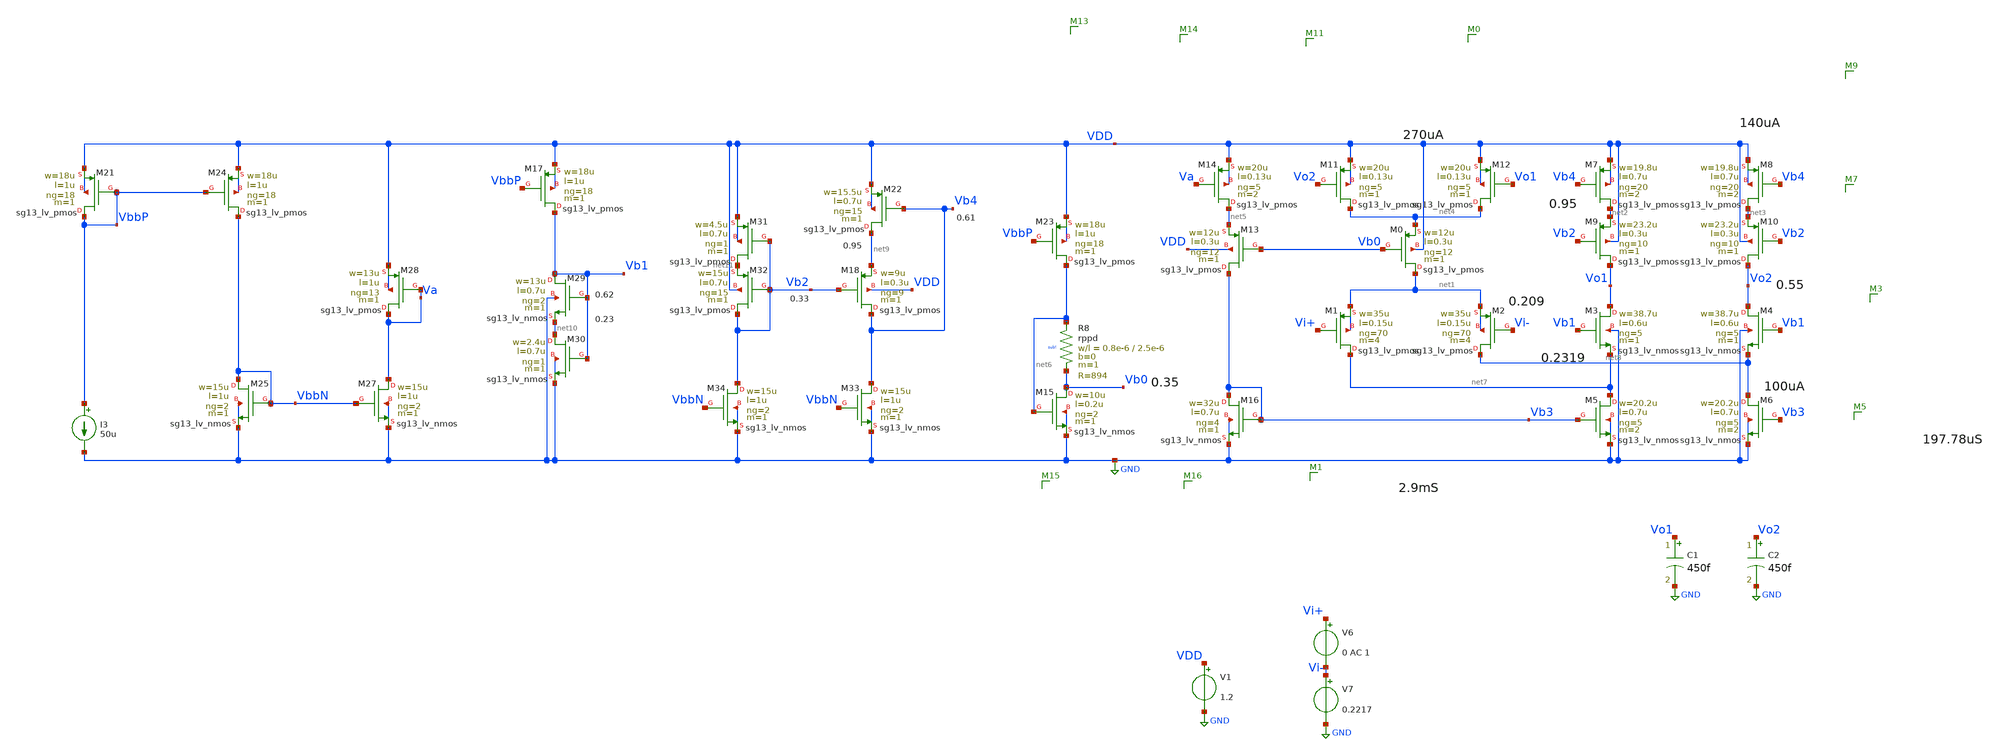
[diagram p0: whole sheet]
** sch_path: sch/testing/gmBoosting.sch
**.subckt gmBoosting
XM7 net2 Vb4 VDD VDD sg13_lv_pmos w=19.8u l=0.7u ng=20 m=2 mm_ok=1
XM1 net7 Vi+ net1 net1 sg13_lv_pmos w=35u l=0.15u ng=70 m=4 mm_ok=1
XM2 net8 Vi- net1 net1 sg13_lv_pmos w=35u l=0.15u ng=70 m=4 mm_ok=1
XM0 net1 Vb0 net4 VDD sg13_lv_pmos w=12u l=0.3u ng=12 m=1 mm_ok=1
V1 VDD GND 1.2
V7 Vi- GND 0.2217
V6 Vi+ Vi- 0 AC 1
C1 Vo1 GND 450f m=1
C2 Vo2 GND 450f m=1
XM9 Vo1 Vb2 net2 VDD sg13_lv_pmos w=23.2u l=0.3u ng=10 m=1 mm_ok=1
XM10 Vo2 Vb2 net3 VDD sg13_lv_pmos w=23.2u l=0.3u ng=10 m=1 mm_ok=1
XM8 net3 Vb4 VDD VDD sg13_lv_pmos w=19.8u l=0.7u ng=20 m=2 mm_ok=1
XM11 net4 Vo2 VDD VDD sg13_lv_pmos w=20u l=0.13u ng=5 m=1 mm_ok=1
XM12 net4 Vo1 VDD VDD sg13_lv_pmos w=20u l=0.13u ng=5 m=1 mm_ok=1
XM14 net5 Va VDD VDD sg13_lv_pmos w=20u l=0.13u ng=5 m=2 mm_ok=1
XM15 Vb0 net6 GND GND sg13_lv_nmos w=10u l=0.2u ng=2 m=1 mm_ok=1
XM16 Vb3 Vb3 GND GND sg13_lv_nmos w=32u l=0.7u ng=4 m=1 mm_ok=1
XR8 net6 Vb0 sub! rppd w=0.8e-6 l=2.5e-6 m=1 b=0 mm_ok=1
XM13 Vb3 Vb0 net5 VDD sg13_lv_pmos w=12u l=0.3u ng=12 m=1 mm_ok=1
I3 VbbP GND 50u
XM21 VbbP VbbP VDD VDD sg13_lv_pmos w=18u l=1u ng=18 m=1 mm_ok=1
XM23 net6 VbbP VDD VDD sg13_lv_pmos w=18u l=1u ng=18 m=1 mm_ok=1
XM24 VbbN VbbP VDD VDD sg13_lv_pmos w=18u l=1u ng=18 m=1 mm_ok=1
XM25 VbbN VbbN GND GND sg13_lv_nmos w=15u l=1u ng=2 m=1 mm_ok=1
XM27 Va VbbN GND GND sg13_lv_nmos w=15u l=1u ng=2 m=1 mm_ok=1
XM28 Va Va VDD VDD sg13_lv_pmos w=13u l=1u ng=13 m=1 mm_ok=1
XM29 Vb1 Vb1 net10 GND sg13_lv_nmos w=13u l=0.7u ng=2 m=1 mm_ok=1
XM30 net10 Vb1 GND GND sg13_lv_nmos w=2.4u l=0.7u ng=1 m=1 mm_ok=1
XM17 Vb1 VbbP VDD VDD sg13_lv_pmos w=18u l=1u ng=18 m=1 mm_ok=1
XM18 Vb4 Vb2 net9 VDD sg13_lv_pmos w=9u l=0.3u ng=9 m=1 mm_ok=1
XM22 net9 Vb4 VDD VDD sg13_lv_pmos w=15.5u l=0.7u ng=15 m=1 mm_ok=1
XM33 Vb4 VbbN GND GND sg13_lv_nmos w=15u l=1u ng=2 m=1 mm_ok=1
XM31 net11 Vb2 VDD VDD sg13_lv_pmos w=4.5u l=0.7u ng=1 m=1 mm_ok=1
XM32 Vb2 Vb2 net11 VDD sg13_lv_pmos w=15u l=0.7u ng=15 m=1 mm_ok=1
XM34 Vb2 VbbN GND GND sg13_lv_nmos w=15u l=1u ng=2 m=1 mm_ok=1
XM3 Vo1 Vb1 net7 GND sg13_lv_nmos w=38.7u l=0.6u ng=5 m=1 mm_ok=1
XM4 Vo2 Vb1 net8 GND sg13_lv_nmos w=38.7u l=0.6u ng=5 m=1 mm_ok=1
XM5 net7 Vb3 GND GND sg13_lv_nmos w=20.2u l=0.7u ng=5 m=2 mm_ok=1
XM6 net8 Vb3 GND GND sg13_lv_nmos w=20.2u l=0.7u ng=5 m=2 mm_ok=1
**** begin user architecture code



.include gmBoosting.save
.lib cornerMOSlv.lib mos_tt
.lib cornerRES.lib res_typ
.temp 65
.control
save all
op
write gmBoosting.raw


ac dec 1k 1 10G
let Av = db((v(Vo1)-v(Vo2)))
meas ac UGBW WHEN Av=0
let phase_vec = 180/pi*cph(v(Vo1)-v(Vo2))

meas ac phase FIND phase_vec WHEN frequency=UGBW
let PM = phase
print PM

plot Av
plot phase_vec



.endc



**** end user architecture code
**.ends
.GLOBAL GND
.end
